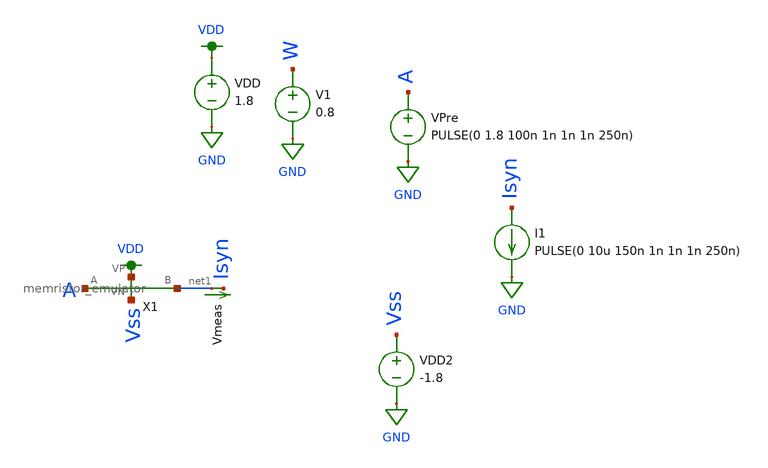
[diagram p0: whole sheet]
** sch_path: schematic/tran_memristor_emulator.sch
**.subckt tran_memristor_emulator
VDD VDD GND 1.8
V1 W GND 0.8
VPre A GND PULSE(0 1.8 100n 1n 1n 1n 250n)
X1 VDD Vss net1 A memristor_emulator
VDD2 Vss GND -1.8
Vmeas net1 Isyn 0
.save i(vmeas)
I1 Isyn GND PULSE(0 10u 150n 1n 1n 1n 250n)
**** begin user architecture code

.param W=1
.param L=0.15
.tran 0.1n 10u
.save all



.option wnflag=1
.param MC_SWITCH=1.0
.lib ~/skywater/skywater-pdk/libraries/sky130_fd_pr_ngspice/latest/models/sky130.lib.spice tt

**** end user architecture code
**.ends

* expanding   symbol:  /home/madvlsi/neuromorphic_computing_final/schematic/memristor_emulator.sym #
*+ of pins=4
** sym_path: schematic/memristor_emulator.sym
** sch_path: schematic/memristor_emulator.sch
.subckt memristor_emulator VP VN B A
*.ipin A
*.iopin VN
*.iopin VP
*.opin B
XM1 B in_cap A B sky130_fd_pr__pfet_01v8 L=0.3 W=12 nf=1 ad='int((nf+1)/2) * W/nf * 0.29' as='int((nf+2)/2) * W/nf * 0.29'
+ pd='2*int((nf+1)/2) * (W/nf + 0.29)' ps='2*int((nf+2)/2) * (W/nf + 0.29)' nrd='0.29 / W' nrs='0.29 / W'
+ sa=0 sb=0 sd=0 mult=1 m=1
XM2 VP A in_cap VP sky130_fd_pr__pfet_01v8 L=2 W=3 nf=1 ad='int((nf+1)/2) * W/nf * 0.29' as='int((nf+2)/2) * W/nf * 0.29'
+ pd='2*int((nf+1)/2) * (W/nf + 0.29)' ps='2*int((nf+2)/2) * (W/nf + 0.29)' nrd='0.29 / W' nrs='0.29 / W'
+ sa=0 sb=0 sd=0 mult=1 m=1
XM3 VN in_cap VN VN sky130_fd_pr__nfet_01v8 L=20 W=20 nf=1 ad='int((nf+1)/2) * W/nf * 0.29' as='int((nf+2)/2) * W/nf * 0.29'
+ pd='2*int((nf+1)/2) * (W/nf + 0.29)' ps='2*int((nf+2)/2) * (W/nf + 0.29)' nrd='0.29 / W' nrs='0.29 / W'
+ sa=0 sb=0 sd=0 mult=1 m=1
XM4 VN B in_cap VN sky130_fd_pr__nfet_01v8 L=3 W=2 nf=1 ad='int((nf+1)/2) * W/nf * 0.29' as='int((nf+2)/2) * W/nf * 0.29'
+ pd='2*int((nf+1)/2) * (W/nf + 0.29)' ps='2*int((nf+2)/2) * (W/nf + 0.29)' nrd='0.29 / W' nrs='0.29 / W'
+ sa=0 sb=0 sd=0 mult=1 m=1
.ends

.GLOBAL GND
.GLOBAL VDD
.end
